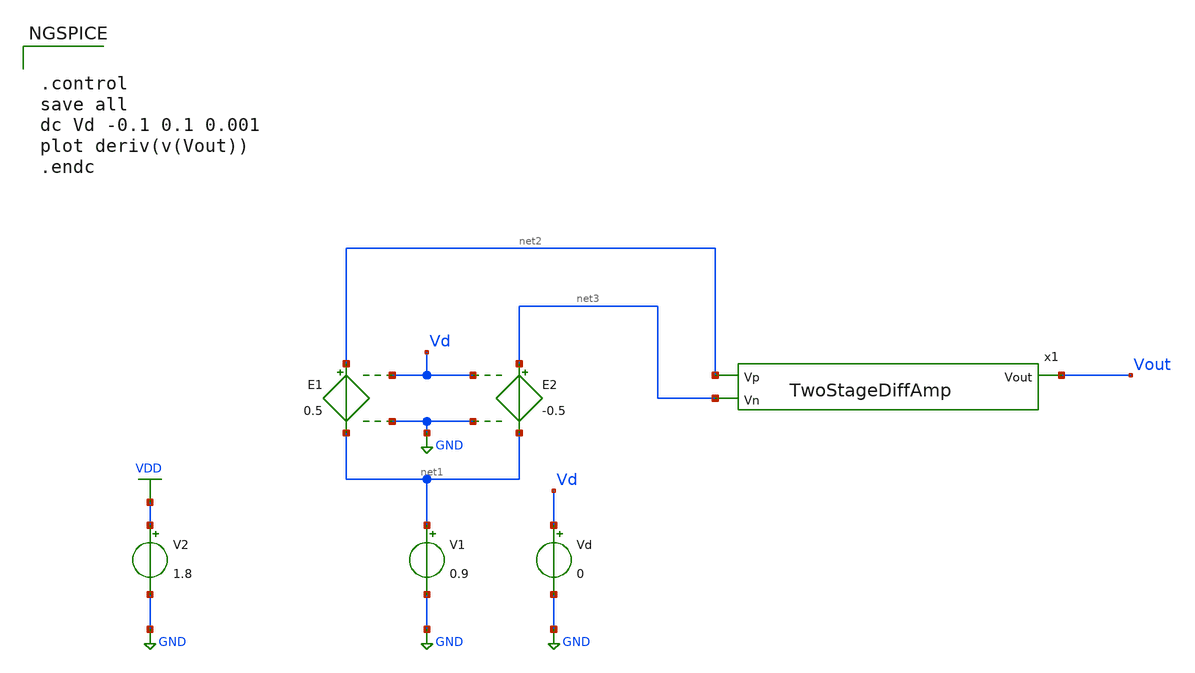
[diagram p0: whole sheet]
** sch_path: Circuits/DiffAmp/DiffAmp_TB.sch
**.subckt DiffAmp_TB
x1 net2 net3 Vout TwoStageDiffAmp
V1 net1 GND 0.9
E1 net2 net1 Vd GND 0.5
E2 net3 net1 Vd GND -0.5
Vd Vd GND 0
V2 VDD GND 1.8
**** begin user architecture code


.control
save all
dc Vd -0.1 0.1 0.001
plot deriv(v(Vout))
.endc



** opencircuitdesign pdks install
.lib $::SKYWATER_MODELS/sky130.lib.spice tt


**** end user architecture code
**.ends
.GLOBAL GND
.GLOBAL VDD
.end
